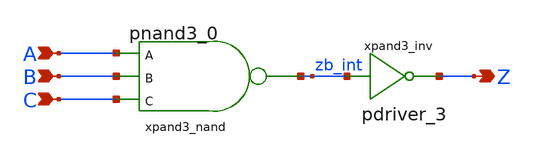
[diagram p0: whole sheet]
** sch_path: sram_2_16_scn4m/pand3_0.sch
**.subckt pand3_0 A B C Z
*.ipin A
*.ipin B
*.ipin C
*.opin Z
xpand3_nand A B C zb_int vdd gnd pnand3_0
xpand3_inv zb_int Z vdd gnd pdriver_3
**.ends
.end
